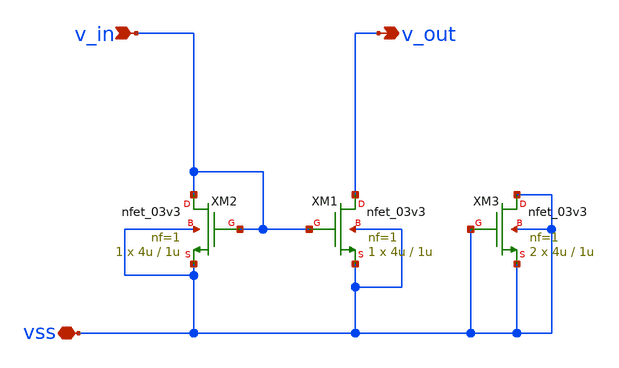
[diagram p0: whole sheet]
** sch_path: blocks/composite/regulated_cascoded_cmirror/xschem/vanilla_cm.sch
**.subckt vanilla_cm v_in vss v_out
*.ipin v_in
*.iopin vss
*.opin v_out
XM1 v_out v_in vss vss nfet_03v3 L=1u W=4u nf=1 ad='int((nf+1)/2) * W/nf * 0.18u' as='int((nf+2)/2) * W/nf * 0.18u'
+ pd='2*int((nf+1)/2) * (W/nf + 0.18u)' ps='2*int((nf+2)/2) * (W/nf + 0.18u)' nrd='0.18u / W' nrs='0.18u / W'
+ sa=0 sb=0 sd=0 m=1
XM2 v_in v_in vss vss nfet_03v3 L=1u W=4u nf=1 ad='int((nf+1)/2) * W/nf * 0.18u' as='int((nf+2)/2) * W/nf * 0.18u'
+ pd='2*int((nf+1)/2) * (W/nf + 0.18u)' ps='2*int((nf+2)/2) * (W/nf + 0.18u)' nrd='0.18u / W' nrs='0.18u / W'
+ sa=0 sb=0 sd=0 m=1
XM3 vss vss vss vss nfet_03v3 L=1u W=4u nf=1 ad='int((nf+1)/2) * W/nf * 0.18u' as='int((nf+2)/2) * W/nf * 0.18u'
+ pd='2*int((nf+1)/2) * (W/nf + 0.18u)' ps='2*int((nf+2)/2) * (W/nf + 0.18u)' nrd='0.18u / W' nrs='0.18u / W'
+ sa=0 sb=0 sd=0 m=2
**.ends
.end
